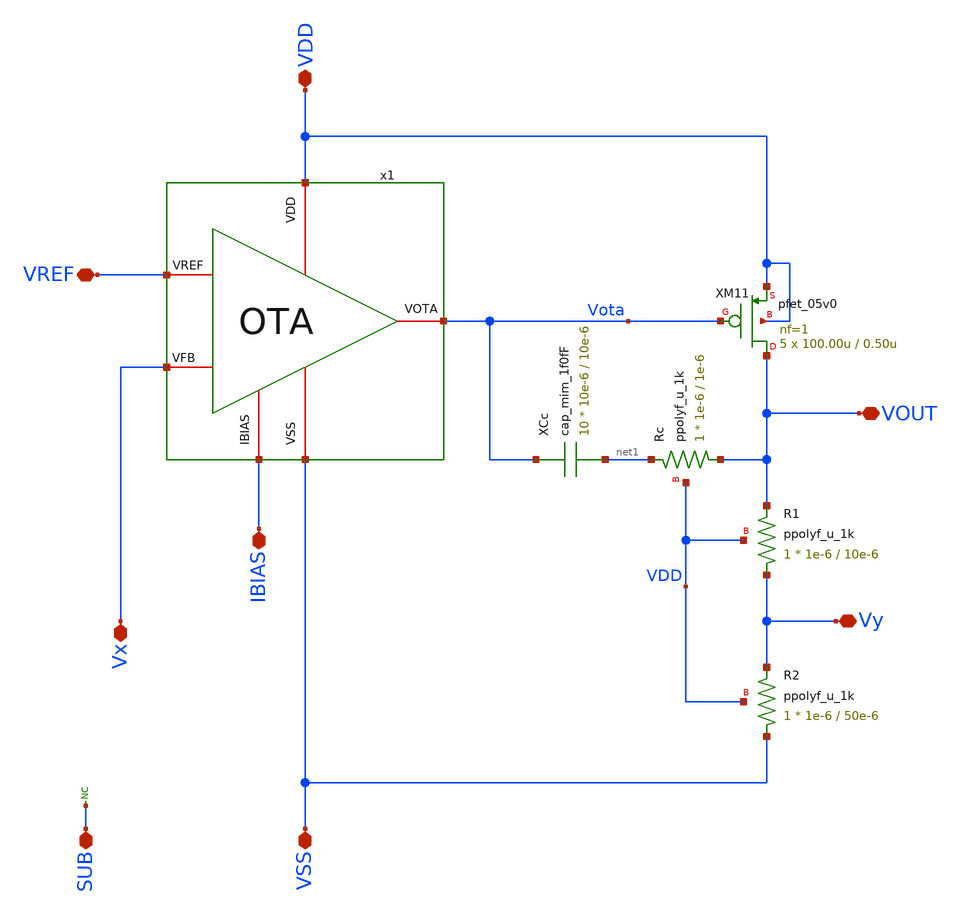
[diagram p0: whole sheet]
** sch_path: designs/libs/core_ldo/ldo/ldo_ldo_OL/ldo_OL.sch
**.subckt ldo_OL VDD VSS VOUT SUB VREF IBIAS Vx Vy
*.iopin VDD
*.iopin VSS
*.iopin VOUT
*.iopin SUB
*.iopin VREF
*.iopin IBIAS
*.iopin Vx
*.iopin Vy
XM11 VOUT Vota VDD VDD pfet_05v0 L=0.50u W=100.00u nf=1 ad='int((nf+1)/2) * W/nf * 0.18u' as='int((nf+2)/2) * W/nf * 0.18u'
+ pd='2*int((nf+1)/2) * (W/nf + 0.18u)' ps='2*int((nf+2)/2) * (W/nf + 0.18u)' nrd='0.18u / W' nrs='0.18u / W'
+ sa=0 sb=0 sd=0 m=5
* noconn SUB
x1 VDD VREF Vx Vota IBIAS VSS OTA
XR1 Vy VOUT VDD ppolyf_u_1k r_width=1e-6 r_length=10e-6 m=1
XR2 VSS Vy VDD ppolyf_u_1k r_width=1e-6 r_length=50e-6 m=1
XRc VOUT net1 VDD ppolyf_u_1k r_width=1e-6 r_length=1e-6 m=1
XCc Vota net1 cap_mim_1f0fF c_width=10e-6 c_length=10e-6 m=10
**.ends

* expanding   symbol:  libs/core_ldo/ldo/ldo_OTA/OTA.sym # of pins=6
** sym_path: designs/libs/core_ldo/ldo/OTA.sym
** sch_path: designs/libs/core_ldo/ldo/OTA.sch
.subckt OTA VDD VREF VFB VOTA IBIAS VSS
*.iopin VDD
*.iopin VSS
*.iopin VOTA
*.iopin VREF
*.iopin IBIAS
*.iopin VFB
XM3 net2 net2 VDD VDD pfet_05v0 L=2.00u W=8.00u nf=1 ad='int((nf+1)/2) * W/nf * 0.18u' as='int((nf+2)/2) * W/nf * 0.18u'
+ pd='2*int((nf+1)/2) * (W/nf + 0.18u)' ps='2*int((nf+2)/2) * (W/nf + 0.18u)' nrd='0.18u / W' nrs='0.18u / W'
+ sa=0 sb=0 sd=0 m=1
XM4 net3 net3 VDD VDD pfet_05v0 L=2.00u W=8.00u nf=1 ad='int((nf+1)/2) * W/nf * 0.18u' as='int((nf+2)/2) * W/nf * 0.18u'
+ pd='2*int((nf+1)/2) * (W/nf + 0.18u)' ps='2*int((nf+2)/2) * (W/nf + 0.18u)' nrd='0.18u / W' nrs='0.18u / W'
+ sa=0 sb=0 sd=0 m=1
XM5 net4 net2 VDD VDD pfet_05v0 L=2.00u W=8.00u nf=1 ad='int((nf+1)/2) * W/nf * 0.18u' as='int((nf+2)/2) * W/nf * 0.18u'
+ pd='2*int((nf+1)/2) * (W/nf + 0.18u)' ps='2*int((nf+2)/2) * (W/nf + 0.18u)' nrd='0.18u / W' nrs='0.18u / W'
+ sa=0 sb=0 sd=0 m=1
XM6 VOTA net3 VDD VDD pfet_05v0 L=2.00u W=8.00u nf=1 ad='int((nf+1)/2) * W/nf * 0.18u' as='int((nf+2)/2) * W/nf * 0.18u'
+ pd='2*int((nf+1)/2) * (W/nf + 0.18u)' ps='2*int((nf+2)/2) * (W/nf + 0.18u)' nrd='0.18u / W' nrs='0.18u / W'
+ sa=0 sb=0 sd=0 m=2
XM9 IBIAS IBIAS VSS VSS nfet_05v0 L=2.00u W=4.00u nf=1 ad='int((nf+1)/2) * W/nf * 0.18u' as='int((nf+2)/2) * W/nf * 0.18u'
+ pd='2*int((nf+1)/2) * (W/nf + 0.18u)' ps='2*int((nf+2)/2) * (W/nf + 0.18u)' nrd='0.18u / W' nrs='0.18u / W'
+ sa=0 sb=0 sd=0 m=1
XM10 net1 IBIAS VSS VSS nfet_05v0 L=2.00u W=4.00u nf=1 ad='int((nf+1)/2) * W/nf * 0.18u' as='int((nf+2)/2) * W/nf * 0.18u'
+ pd='2*int((nf+1)/2) * (W/nf + 0.18u)' ps='2*int((nf+2)/2) * (W/nf + 0.18u)' nrd='0.18u / W' nrs='0.18u / W'
+ sa=0 sb=0 sd=0 m=1
XM7 net4 net4 VSS VSS nfet_05v0 L=2.00u W=4.00u nf=1 ad='int((nf+1)/2) * W/nf * 0.18u' as='int((nf+2)/2) * W/nf * 0.18u'
+ pd='2*int((nf+1)/2) * (W/nf + 0.18u)' ps='2*int((nf+2)/2) * (W/nf + 0.18u)' nrd='0.18u / W' nrs='0.18u / W'
+ sa=0 sb=0 sd=0 m=1
XM8 VOTA net4 VSS VSS nfet_05v0 L=2.00u W=4.00u nf=1 ad='int((nf+1)/2) * W/nf * 0.18u' as='int((nf+2)/2) * W/nf * 0.18u'
+ pd='2*int((nf+1)/2) * (W/nf + 0.18u)' ps='2*int((nf+2)/2) * (W/nf + 0.18u)' nrd='0.18u / W' nrs='0.18u / W'
+ sa=0 sb=0 sd=0 m=2
XM1 net2 VREF net1 net1 nfet_05v0 L=0.60u W=40.00u nf=1 ad='int((nf+1)/2) * W/nf * 0.18u' as='int((nf+2)/2) * W/nf * 0.18u'
+ pd='2*int((nf+1)/2) * (W/nf + 0.18u)' ps='2*int((nf+2)/2) * (W/nf + 0.18u)' nrd='0.18u / W' nrs='0.18u / W'
+ sa=0 sb=0 sd=0 m=1
XM2 net3 VFB net1 net1 nfet_05v0 L=0.60u W=40.00u nf=1 ad='int((nf+1)/2) * W/nf * 0.18u' as='int((nf+2)/2) * W/nf * 0.18u'
+ pd='2*int((nf+1)/2) * (W/nf + 0.18u)' ps='2*int((nf+2)/2) * (W/nf + 0.18u)' nrd='0.18u / W' nrs='0.18u / W'
+ sa=0 sb=0 sd=0 m=1
.ends

.end
